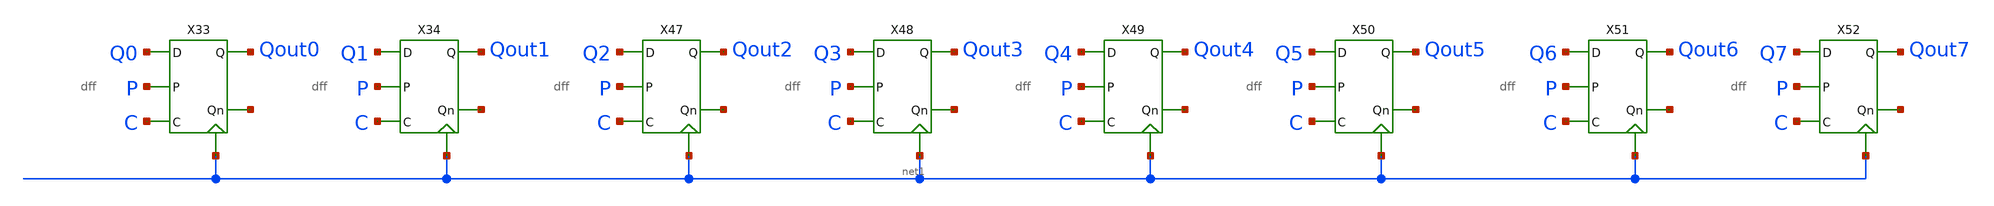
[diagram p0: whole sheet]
** sch_path: schematic/output_register_lvs.sch
**.subckt output_register_lvs
X33 Q0 net2 Qout0 net1 P C dff
X34 Q1 net3 Qout1 net1 P C dff
X47 Q2 net4 Qout2 net1 P C dff
X48 Q3 net5 Qout3 net1 P C dff
X49 Q4 net6 Qout4 net1 P C dff
X50 Q5 net7 Qout5 net1 P C dff
X51 Q6 net8 Qout6 net1 P C dff
X52 Q7 net9 Qout7 net1 P C dff
**.ends
.end
